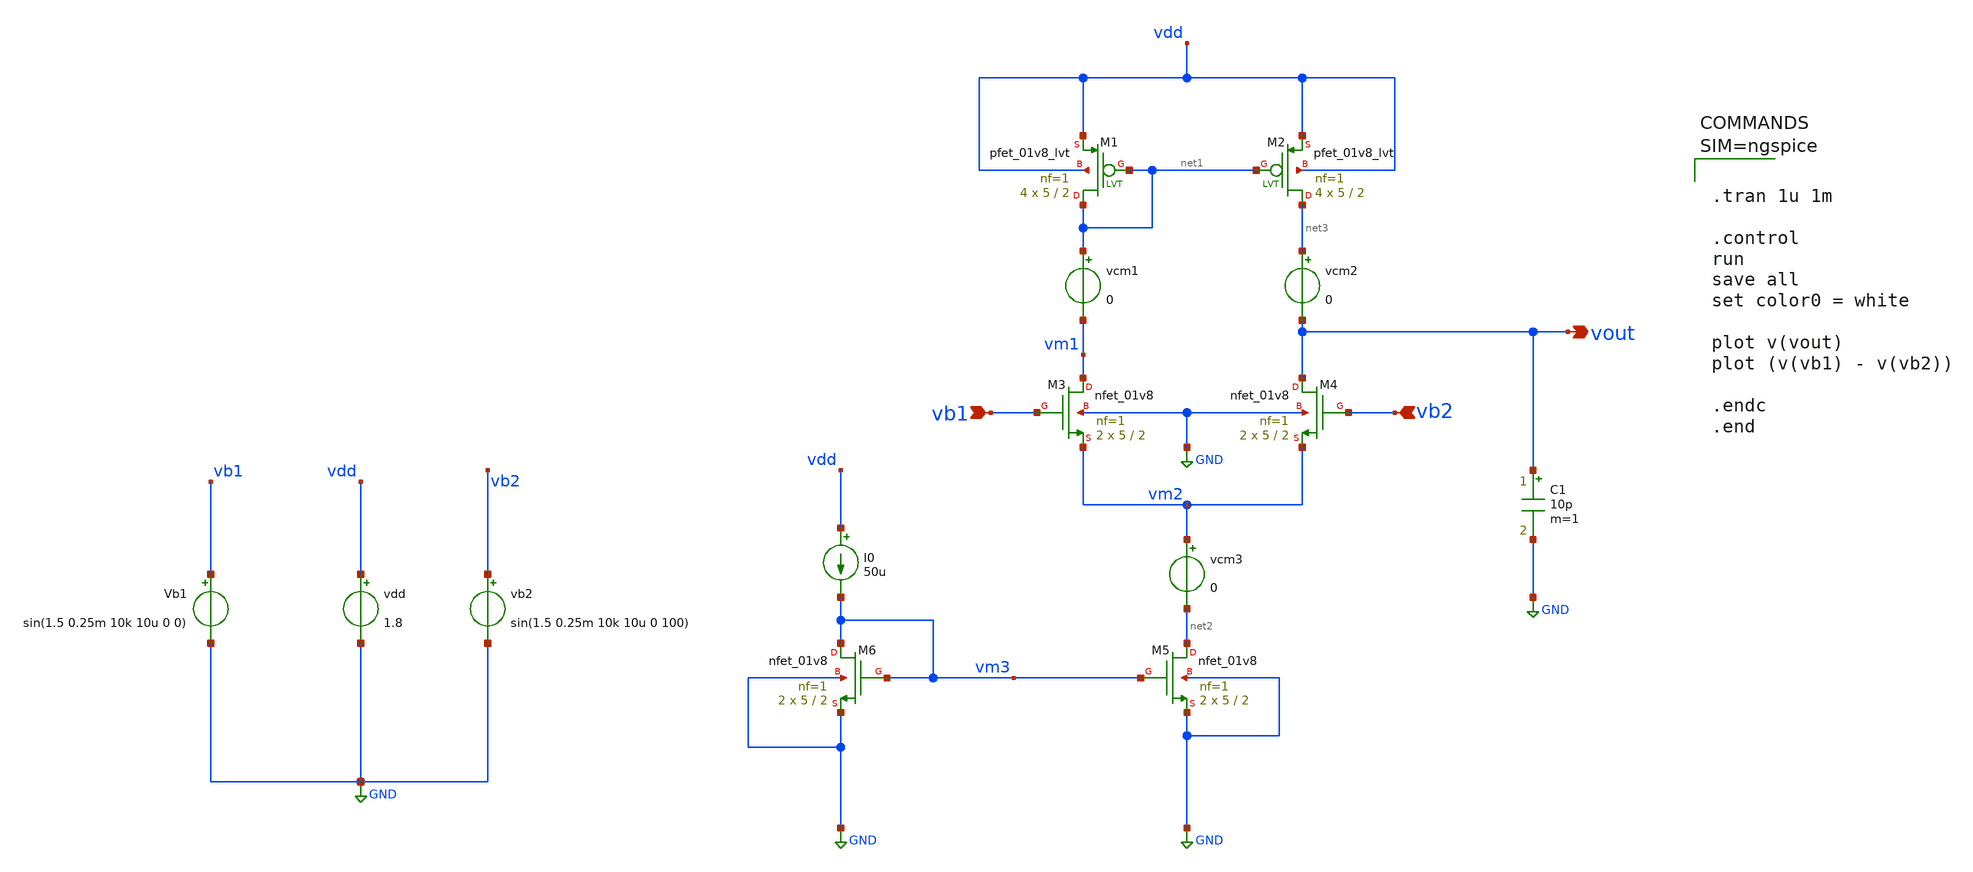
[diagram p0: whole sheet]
** sch_path: testbenches/Differential_Amplifier_AC_transient.sch
**.subckt Differential_Amplifier_AC_transient vout vb1 vb2
*.opin vout
*.ipin vb1
*.ipin vb2
XM5 net2 vm3 GND GND sky130_fd_pr__nfet_01v8 L=2 W=5 nf=1 ad='int((1 + 1)/2) * 5 / 1 * 0.29' as='int((1 + 2)/2) * 5 / 1 * 0.29'
+ pd='2*int((1 + 1)/2) * (5 / 1 + 0.29)' ps='2*int((1 + 2)/2) * (5 / 1 + 0.29)' nrd='0.29 / 5 ' nrs='0.29 / 5 '
+ sa=0 sb=0 sd=0 mult=2 m=2
I0 vdd vm3 50u
vdd vdd GND 1.8
Vb1 vb1 GND sin(1.5 0.25m 10k 10u 0 0)
XM2 net3 net1 vdd vdd sky130_fd_pr__pfet_01v8_lvt L=2 W=5 nf=1 ad='int((1 + 1)/2) * 5 / 1 * 0.29' as='int((1 + 2)/2) * 5 / 1 * 0.29'
+ pd='2*int((1 + 1)/2) * (5 / 1 + 0.29)' ps='2*int((1 + 2)/2) * (5 / 1 + 0.29)' nrd='0.29 / 5 ' nrs='0.29 / 5 '
+ sa=0 sb=0 sd=0 mult=4 m=4
XM3 vm1 vb1 vm2 GND sky130_fd_pr__nfet_01v8 L=2 W=5 nf=1 ad='int((1 + 1)/2) * 5 / 1 * 0.29' as='int((1 + 2)/2) * 5 / 1 * 0.29'
+ pd='2*int((1 + 1)/2) * (5 / 1 + 0.29)' ps='2*int((1 + 2)/2) * (5 / 1 + 0.29)' nrd='0.29 / 5 ' nrs='0.29 / 5 '
+ sa=0 sb=0 sd=0 mult=2 m=2
XM4 vout vb2 vm2 GND sky130_fd_pr__nfet_01v8 L=2 W=5 nf=1 ad='int((1 + 1)/2) * 5 / 1 * 0.29' as='int((1 + 2)/2) * 5 / 1 * 0.29'
+ pd='2*int((1 + 1)/2) * (5 / 1 + 0.29)' ps='2*int((1 + 2)/2) * (5 / 1 + 0.29)' nrd='0.29 / 5 ' nrs='0.29 / 5 '
+ sa=0 sb=0 sd=0 mult=2 m=2
XM6 vm3 vm3 GND GND sky130_fd_pr__nfet_01v8 L=2 W=5 nf=1 ad='int((1 + 1)/2) * 5 / 1 * 0.29' as='int((1 + 2)/2) * 5 / 1 * 0.29'
+ pd='2*int((1 + 1)/2) * (5 / 1 + 0.29)' ps='2*int((1 + 2)/2) * (5 / 1 + 0.29)' nrd='0.29 / 5 ' nrs='0.29 / 5 '
+ sa=0 sb=0 sd=0 mult=2 m=2
XM1 net1 net1 vdd vdd sky130_fd_pr__pfet_01v8_lvt L=2 W=5 nf=1 ad='int((1 + 1)/2) * 5 / 1 * 0.29' as='int((1 + 2)/2) * 5 / 1 * 0.29'
+ pd='2*int((1 + 1)/2) * (5 / 1 + 0.29)' ps='2*int((1 + 2)/2) * (5 / 1 + 0.29)' nrd='0.29 / 5 ' nrs='0.29 / 5 '
+ sa=0 sb=0 sd=0 mult=4 m=4
vcm3 vm2 net2 0
vcm1 net1 vm1 0
vcm2 net3 vout 0
C1 vout GND 10p m=1
vb2 vb2 GND sin(1.5 0.25m 10k 10u 0 100)
**** begin user architecture code

** opencircuitdesign pdks install
.lib $::SKYWATER_MODELS/sky130.lib.spice tt




.tran 1u 1m

.control
run
save all
set color0 = white

plot v(vout)
plot (v(vb1) - v(vb2))

.endc
.end




**** end user architecture code
**.ends
.GLOBAL GND
.end
